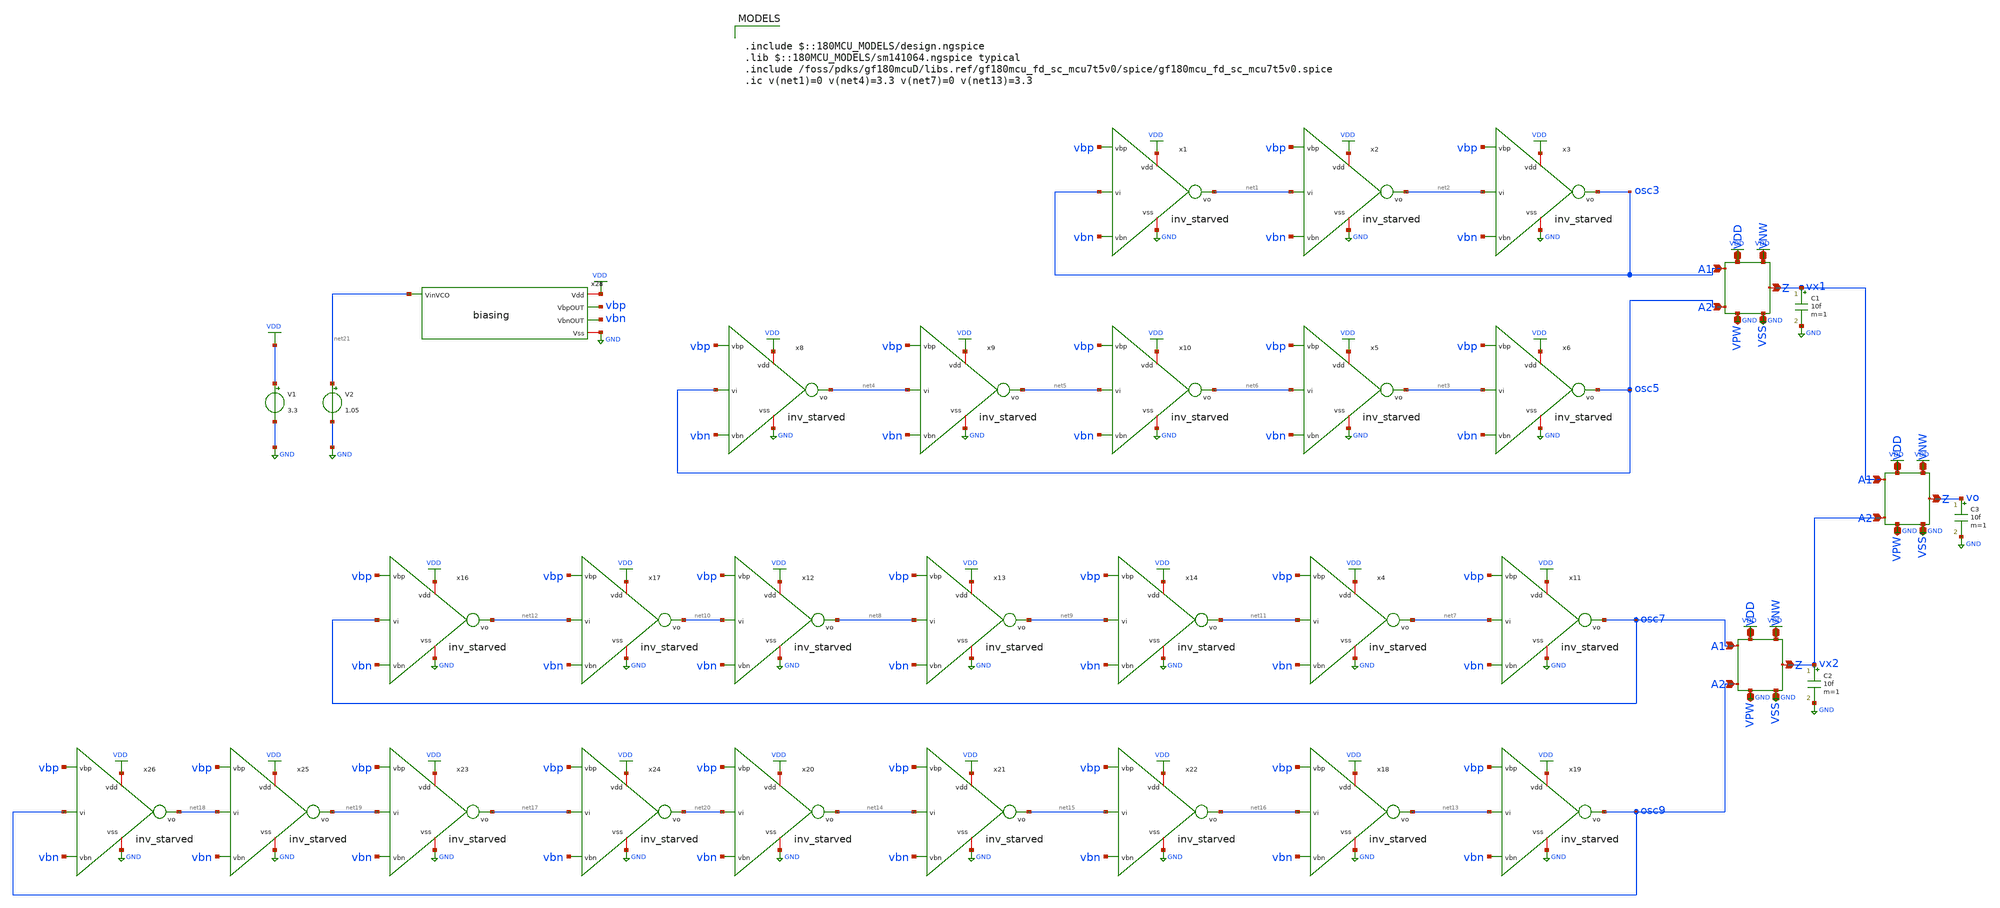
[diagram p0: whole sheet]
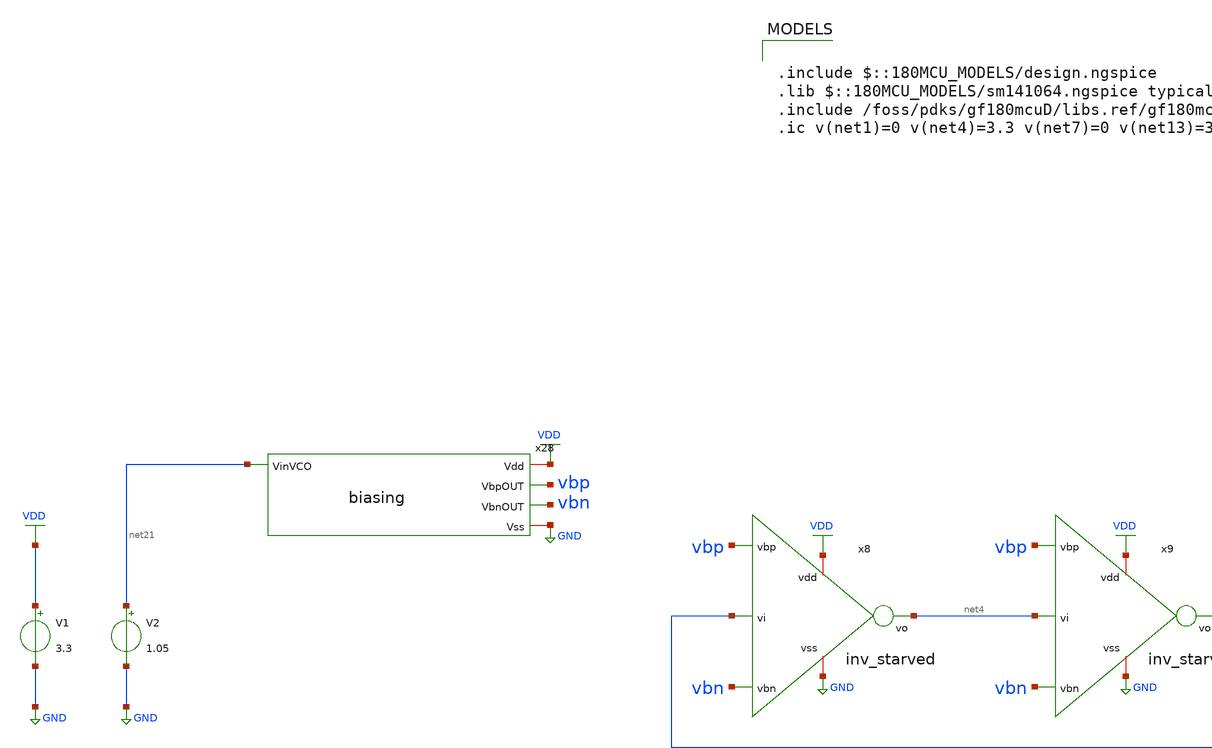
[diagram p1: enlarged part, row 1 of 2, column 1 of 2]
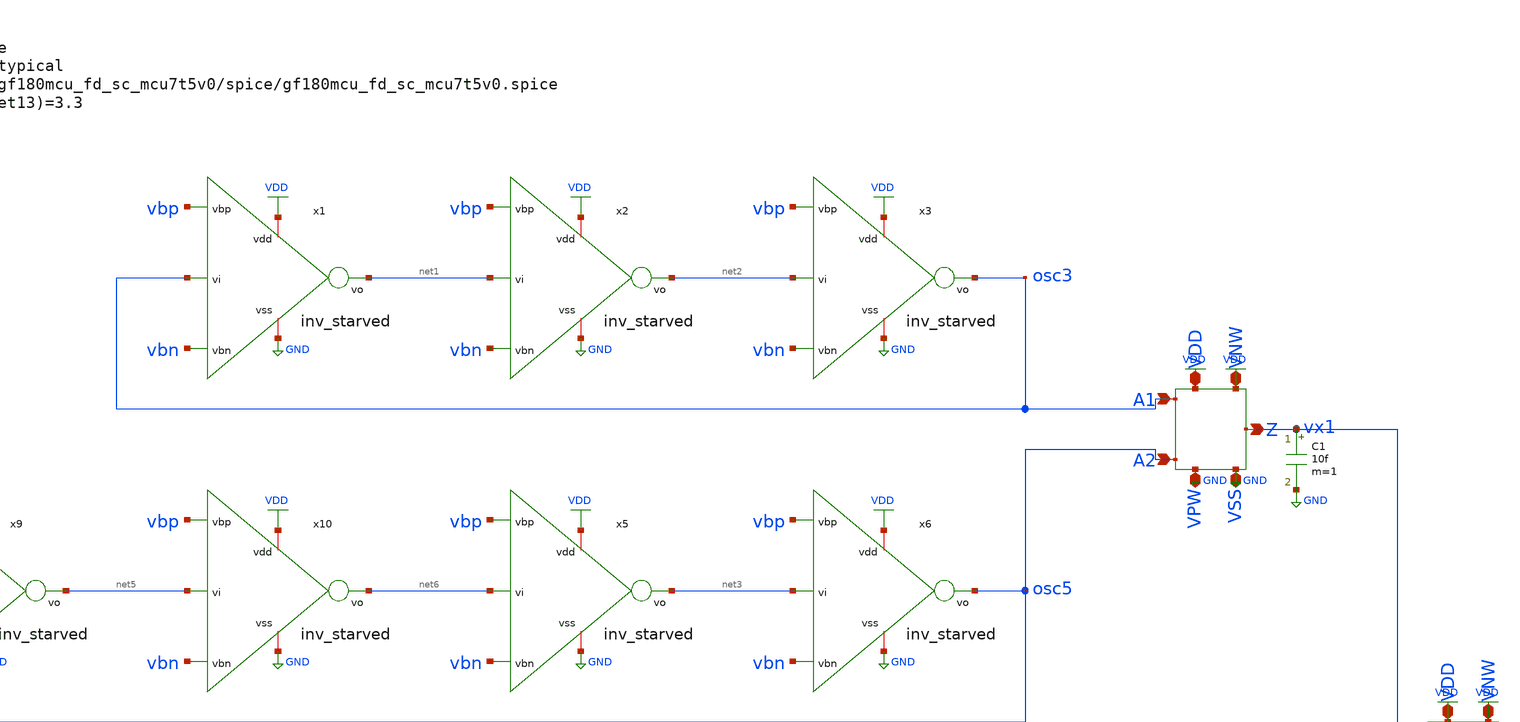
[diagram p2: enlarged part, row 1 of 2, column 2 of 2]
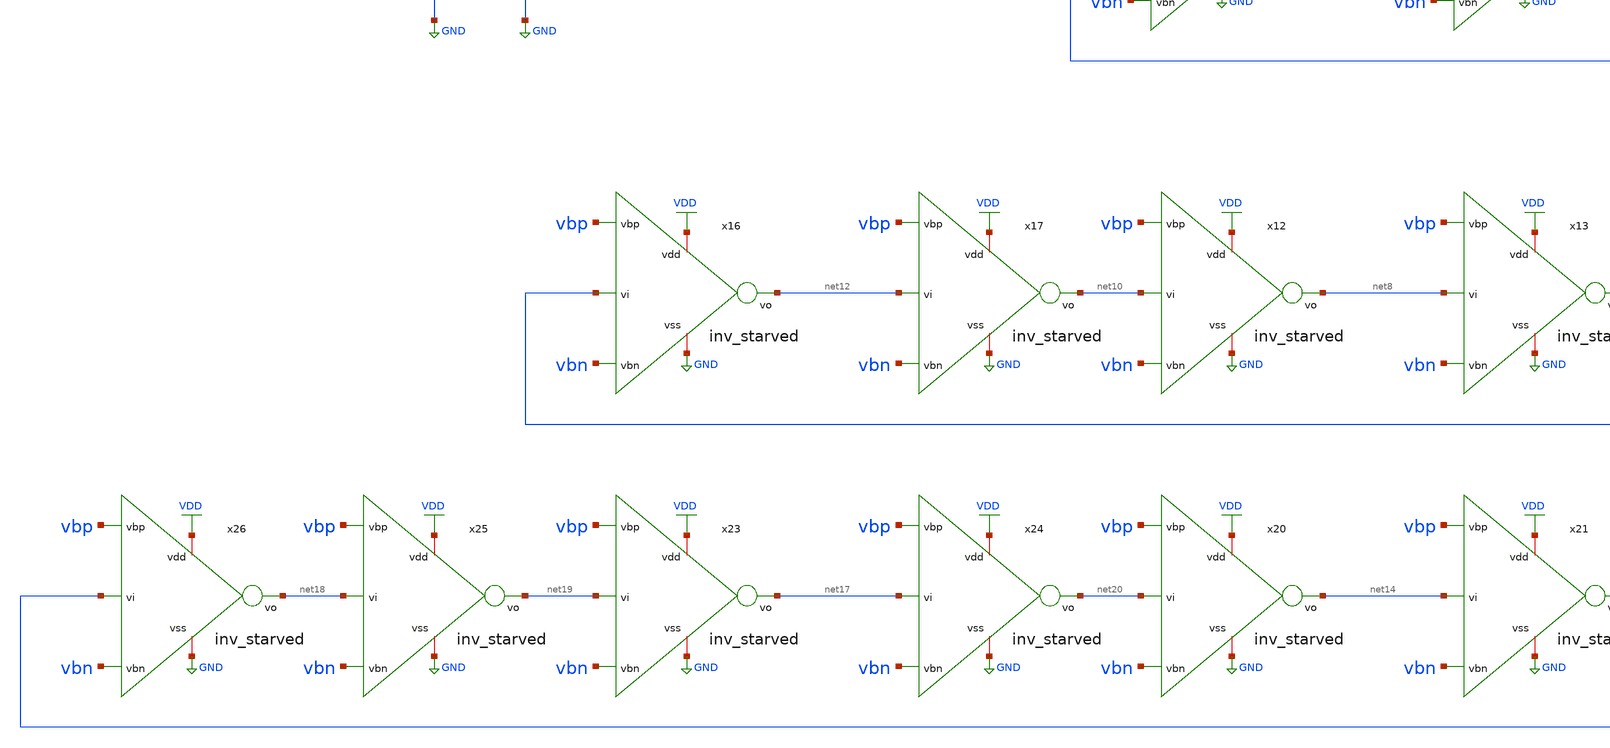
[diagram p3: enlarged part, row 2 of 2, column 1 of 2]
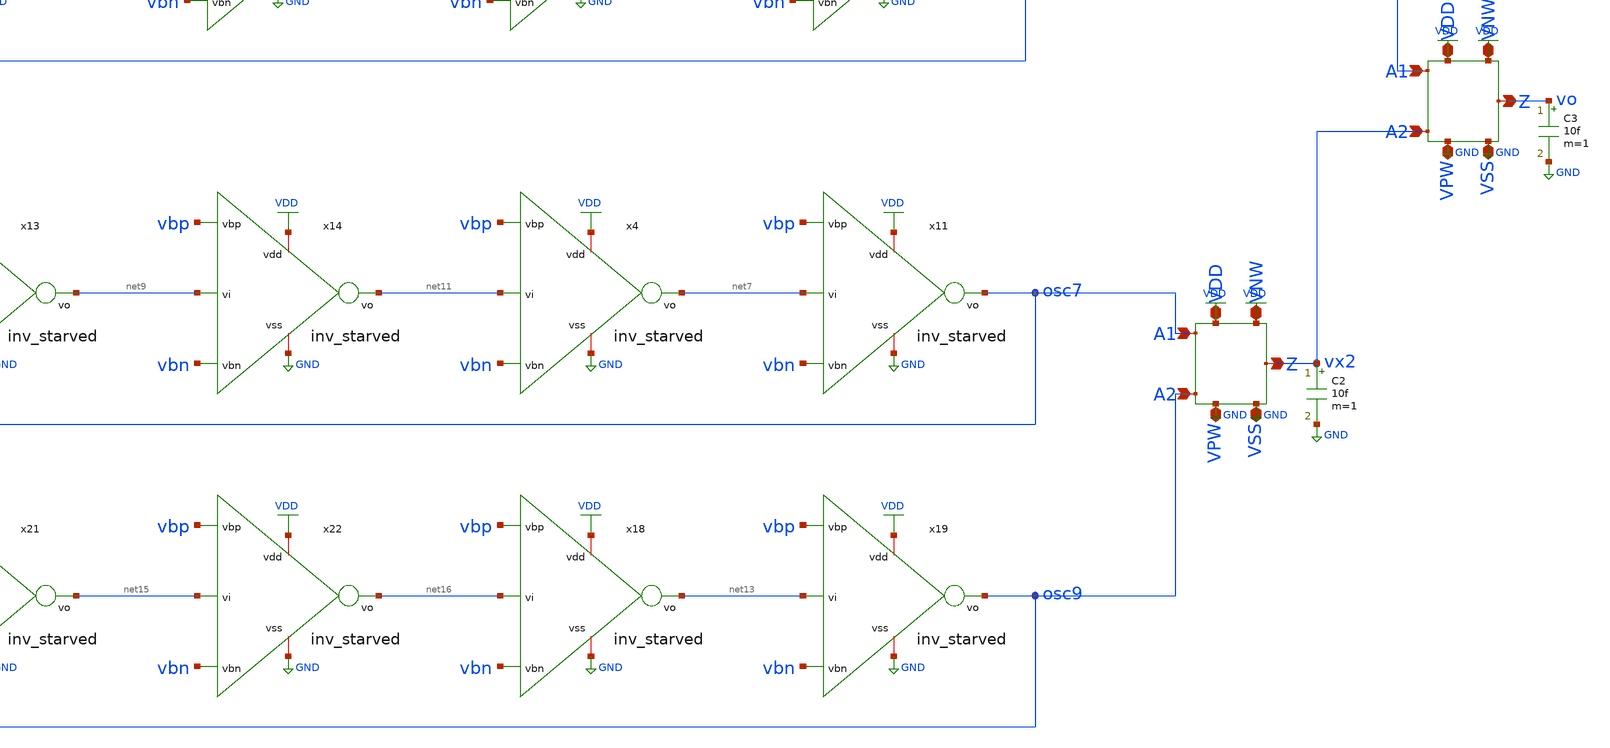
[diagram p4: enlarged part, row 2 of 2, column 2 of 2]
** sch_path: src/analog/inv_starved_tb.sch
**.subckt inv_starved_tb
x1 VDD vbp osc3 net1 vbn GND inv_starved
V1 VDD GND 3.3
x2 VDD vbp net1 net2 vbn GND inv_starved
x3 VDD vbp net2 osc3 vbn GND inv_starved
x5 VDD vbp net6 net3 vbn GND inv_starved
x6 VDD vbp net3 osc5 vbn GND inv_starved
C1 vx1 GND 10f m=1
x8 VDD vbp osc5 net4 vbn GND inv_starved
x9 VDD vbp net4 net5 vbn GND inv_starved
x10 VDD vbp net5 net6 vbn GND inv_starved
x4 VDD vbp net11 net7 vbn GND inv_starved
x11 VDD vbp net7 osc7 vbn GND inv_starved
x12 VDD vbp net10 net8 vbn GND inv_starved
x13 VDD vbp net8 net9 vbn GND inv_starved
x14 VDD vbp net9 net11 vbn GND inv_starved
x16 VDD vbp osc7 net12 vbn GND inv_starved
x17 VDD vbp net12 net10 vbn GND inv_starved
C2 vx2 GND 10f m=1
x18 VDD vbp net16 net13 vbn GND inv_starved
x19 VDD vbp net13 osc9 vbn GND inv_starved
x20 VDD vbp net20 net14 vbn GND inv_starved
x21 VDD vbp net14 net15 vbn GND inv_starved
x22 VDD vbp net15 net16 vbn GND inv_starved
x23 VDD vbp net19 net17 vbn GND inv_starved
x24 VDD vbp net17 net20 vbn GND inv_starved
x25 VDD vbp net18 net19 vbn GND inv_starved
x26 VDD vbp osc9 net18 vbn GND inv_starved
C3 vo GND 10f m=1
x28 VDD vbp vbn net21 GND biasing
V2 net21 GND 1.05
**** begin user architecture code

.include $::180MCU_MODELS/design.ngspice
.lib $::180MCU_MODELS/sm141064.ngspice typical
.include /foss/pdks/gf180mcuD/libs.ref/gf180mcu_fd_sc_mcu7t5v0/spice/gf180mcu_fd_sc_mcu7t5v0.spice
.ic v(net1)=0 v(net4)=3.3 v(net7)=0 v(net13)=3.3



.control
set ngbehavior=hsa

save v(vo) v(osc3) v(osc5) v(osc7) v(osc9)

** Run
tran 100p 100u

** Write data to project directory
wrdata /foss/designs/trng_analog/current_starved/ro_data.txt v(vo) v(osc3) v(osc5) v(osc7) v(osc9)

** plot v(osc3) v(osc5) v(vo)+4 v(osc7) v(osc9)
.endc


**** end user architecture code
**.ends

* expanding   symbol:  inv_starved.sym # of pins=6
** sym_path: src/analog/inv_starved.sym
** sch_path: src/analog/inv_starved.sch
.subckt inv_starved vdd vbp vi vo vbn vss
*.iopin vdd
*.iopin vss
*.ipin vi
*.opin vo
*.ipin vbp
*.ipin vbn
XM1 vo vi net2 vss nfet_03v3 L=0.28u W=1u nf=1 ad='int((nf+1)/2) * W/nf * 0.18u' as='int((nf+2)/2) * W/nf * 0.18u'
+ pd='2*int((nf+1)/2) * (W/nf + 0.18u)' ps='2*int((nf+2)/2) * (W/nf + 0.18u)' nrd='0.18u / W' nrs='0.18u / W'
+ sa=0 sb=0 sd=0 m=1
XM2 vo vi net1 vdd pfet_03v3 L=0.28u W=2u nf=1 ad='int((nf+1)/2) * W/nf * 0.18u' as='int((nf+2)/2) * W/nf * 0.18u'
+ pd='2*int((nf+1)/2) * (W/nf + 0.18u)' ps='2*int((nf+2)/2) * (W/nf + 0.18u)' nrd='0.18u / W' nrs='0.18u / W'
+ sa=0 sb=0 sd=0 m=1
XM3 net1 vbp vdd vdd pfet_03v3 L=0.5u W=2u nf=1 ad='int((nf+1)/2) * W/nf * 0.18u' as='int((nf+2)/2) * W/nf * 0.18u'
+ pd='2*int((nf+1)/2) * (W/nf + 0.18u)' ps='2*int((nf+2)/2) * (W/nf + 0.18u)' nrd='0.18u / W' nrs='0.18u / W'
+ sa=0 sb=0 sd=0 m=1
XM4 net2 vbn vss vss nfet_03v3 L=0.5u W=1u nf=1 ad='int((nf+1)/2) * W/nf * 0.18u' as='int((nf+2)/2) * W/nf * 0.18u'
+ pd='2*int((nf+1)/2) * (W/nf + 0.18u)' ps='2*int((nf+2)/2) * (W/nf + 0.18u)' nrd='0.18u / W' nrs='0.18u / W'
+ sa=0 sb=0 sd=0 m=1
.ends


* expanding   symbol:  biasing.sym # of pins=5
** sym_path: src/analog/biasing.sym
** sch_path: src/analog/biasing.sch
.subckt biasing Vdd VbpOUT VbnOUT VinVCO Vss
*.iopin Vdd
*.iopin Vss
*.ipin VinVCO
*.opin VbpOUT
*.opin VbnOUT
XM3 VbpOUT VbpOUT Vdd Vdd pfet_03v3 L=0.5u W=2u nf=1 ad='int((nf+1)/2) * W/nf * 0.18u' as='int((nf+2)/2) * W/nf * 0.18u'
+ pd='2*int((nf+1)/2) * (W/nf + 0.18u)' ps='2*int((nf+2)/2) * (W/nf + 0.18u)' nrd='0.18u / W' nrs='0.18u / W'
+ sa=0 sb=0 sd=0 m=1
XM4 VbpOUT VinVCO Vss Vss nfet_03v3 L=0.5u W=1u nf=1 ad='int((nf+1)/2) * W/nf * 0.18u' as='int((nf+2)/2) * W/nf * 0.18u'
+ pd='2*int((nf+1)/2) * (W/nf + 0.18u)' ps='2*int((nf+2)/2) * (W/nf + 0.18u)' nrd='0.18u / W' nrs='0.18u / W'
+ sa=0 sb=0 sd=0 m=1
XM1 VbnOUT VbpOUT Vdd Vdd pfet_03v3 L=0.5u W=2u nf=1 ad='int((nf+1)/2) * W/nf * 0.18u' as='int((nf+2)/2) * W/nf * 0.18u'
+ pd='2*int((nf+1)/2) * (W/nf + 0.18u)' ps='2*int((nf+2)/2) * (W/nf + 0.18u)' nrd='0.18u / W' nrs='0.18u / W'
+ sa=0 sb=0 sd=0 m=1
XM2 VbnOUT VbnOUT Vss Vss nfet_03v3 L=0.5u W=1u nf=1 ad='int((nf+1)/2) * W/nf * 0.18u' as='int((nf+2)/2) * W/nf * 0.18u'
+ pd='2*int((nf+1)/2) * (W/nf + 0.18u)' ps='2*int((nf+2)/2) * (W/nf + 0.18u)' nrd='0.18u / W' nrs='0.18u / W'
+ sa=0 sb=0 sd=0 m=1
.ends

.GLOBAL VDD
.GLOBAL GND
.end
